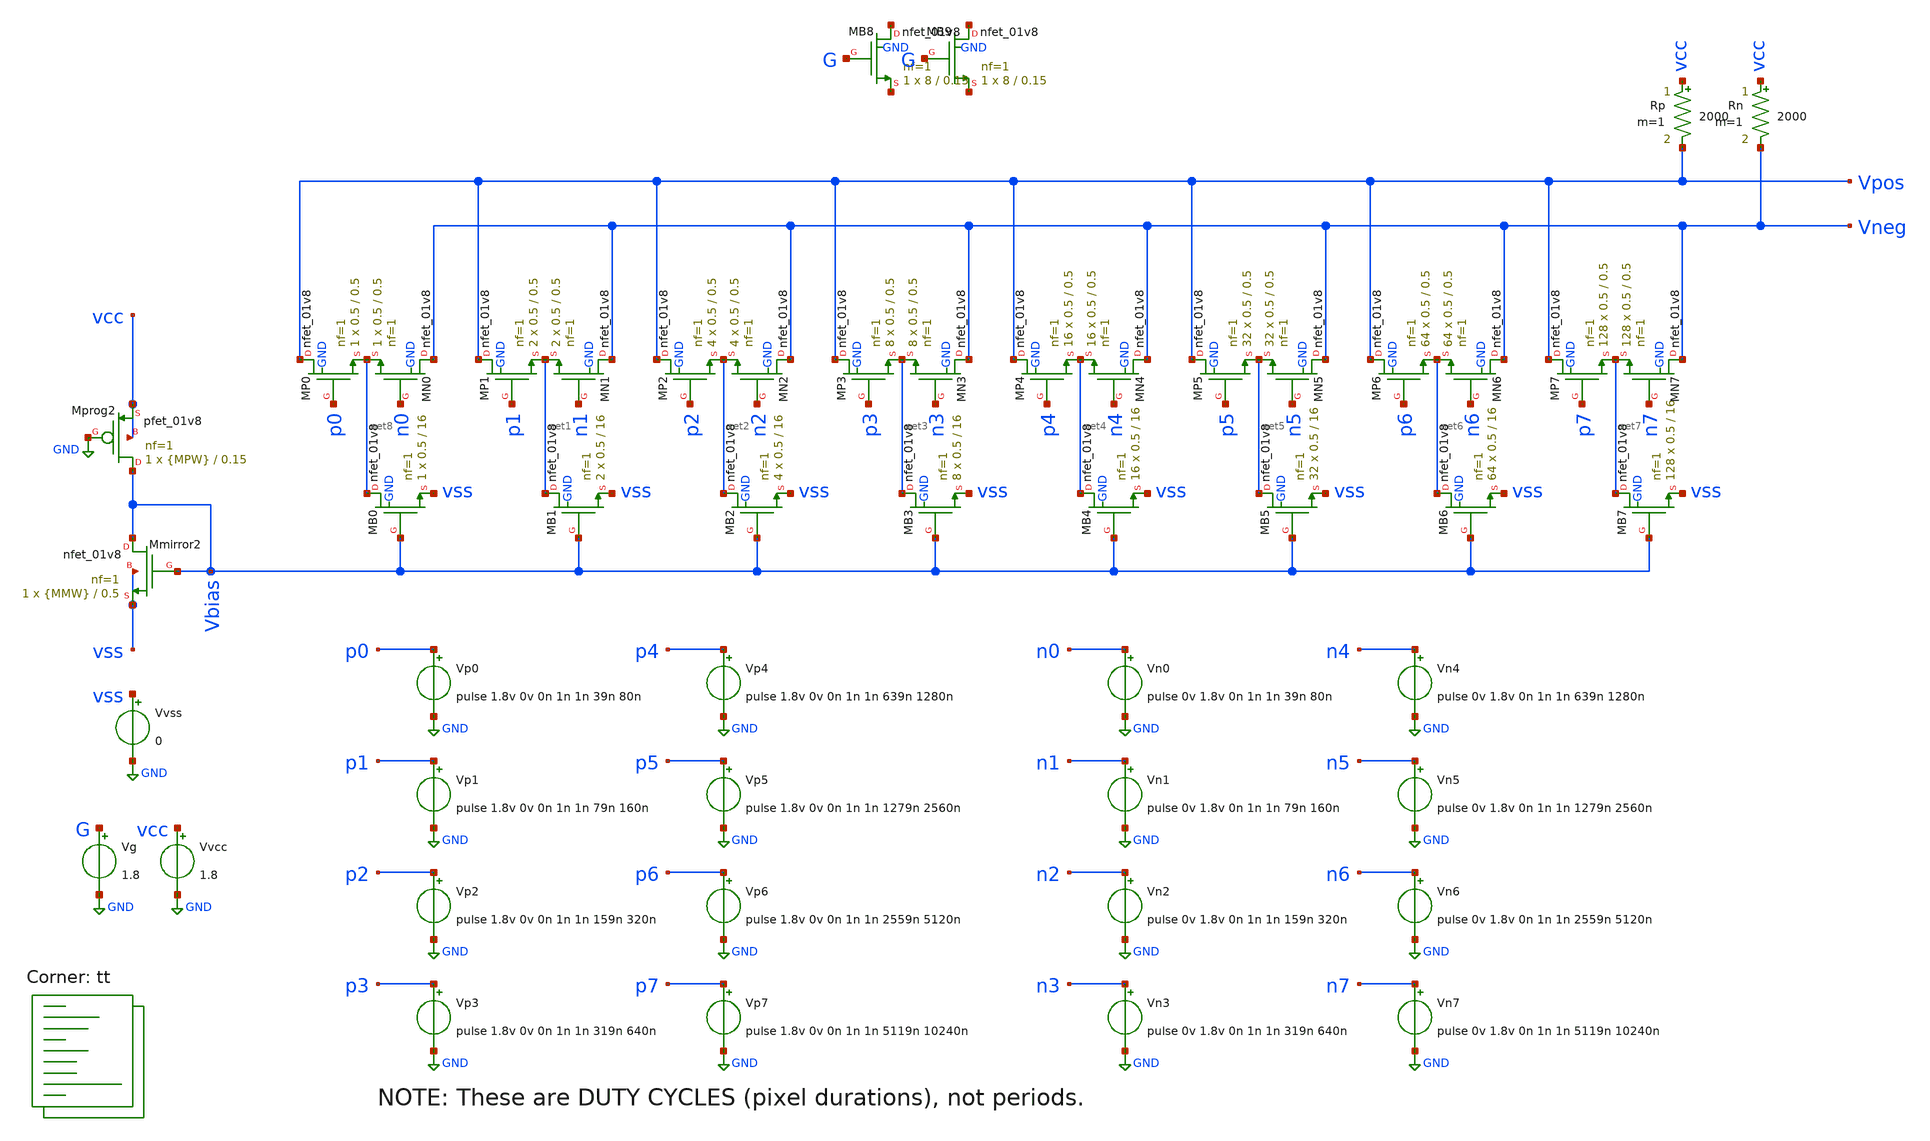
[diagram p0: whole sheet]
** sch_path: xschem/10-steer.sch
**.subckt 10-steer
Vvcc vcc GND 1.8
Vg G GND 1.8
XMprog2 Vbias GND vcc vcc sky130_fd_pr__pfet_01v8 L=0.15 W={MPW} nf=1 ad='int((nf+1)/2) * W/nf * 0.29'
+ as='int((nf+2)/2) * W/nf * 0.29' pd='2*int((nf+1)/2) * (W/nf + 0.29)' ps='2*int((nf+2)/2) * (W/nf + 0.29)'
+ nrd='0.29 / W' nrs='0.29 / W' sa=0 sb=0 sd=0 mult=1 m=1
XMmirror2 Vbias Vbias vss vss sky130_fd_pr__nfet_01v8 L=0.5 W={MMW} nf=1 ad='int((nf+1)/2) * W/nf * 0.29'
+ as='int((nf+2)/2) * W/nf * 0.29' pd='2*int((nf+1)/2) * (W/nf + 0.29)' ps='2*int((nf+2)/2) * (W/nf + 0.29)'
+ nrd='0.29 / W' nrs='0.29 / W' sa=0 sb=0 sd=0 mult=1 m=1
XMB0 net8 Vbias vss GND sky130_fd_pr__nfet_01v8 L=16 W=0.5 nf=1 ad='int((nf+1)/2) * W/nf * 0.29' as='int((nf+2)/2) * W/nf * 0.29'
+ pd='2*int((nf+1)/2) * (W/nf + 0.29)' ps='2*int((nf+2)/2) * (W/nf + 0.29)' nrd='0.29 / W' nrs='0.29 / W'
+ sa=0 sb=0 sd=0 mult=1 m=1
XMP0 Vpos p0 net8 GND sky130_fd_pr__nfet_01v8 L=0.5 W=0.5 nf=1 ad='int((nf+1)/2) * W/nf * 0.29' as='int((nf+2)/2) * W/nf * 0.29'
+ pd='2*int((nf+1)/2) * (W/nf + 0.29)' ps='2*int((nf+2)/2) * (W/nf + 0.29)' nrd='0.29 / W' nrs='0.29 / W'
+ sa=0 sb=0 sd=0 mult=1 m=1
XMN0 Vneg n0 net8 GND sky130_fd_pr__nfet_01v8 L=0.5 W=0.5 nf=1 ad='int((nf+1)/2) * W/nf * 0.29' as='int((nf+2)/2) * W/nf * 0.29'
+ pd='2*int((nf+1)/2) * (W/nf + 0.29)' ps='2*int((nf+2)/2) * (W/nf + 0.29)' nrd='0.29 / W' nrs='0.29 / W'
+ sa=0 sb=0 sd=0 mult=1 m=1
XMB1 net1 Vbias vss GND sky130_fd_pr__nfet_01v8 L=16 W=0.5 nf=1 ad='int((nf+1)/2) * W/nf * 0.29' as='int((nf+2)/2) * W/nf * 0.29'
+ pd='2*int((nf+1)/2) * (W/nf + 0.29)' ps='2*int((nf+2)/2) * (W/nf + 0.29)' nrd='0.29 / W' nrs='0.29 / W'
+ sa=0 sb=0 sd=0 mult=2 m=2
XMP1 Vpos p1 net1 GND sky130_fd_pr__nfet_01v8 L=0.5 W=0.5 nf=1 ad='int((nf+1)/2) * W/nf * 0.29' as='int((nf+2)/2) * W/nf * 0.29'
+ pd='2*int((nf+1)/2) * (W/nf + 0.29)' ps='2*int((nf+2)/2) * (W/nf + 0.29)' nrd='0.29 / W' nrs='0.29 / W'
+ sa=0 sb=0 sd=0 mult=2 m=2
XMN1 Vneg n1 net1 GND sky130_fd_pr__nfet_01v8 L=0.5 W=0.5 nf=1 ad='int((nf+1)/2) * W/nf * 0.29' as='int((nf+2)/2) * W/nf * 0.29'
+ pd='2*int((nf+1)/2) * (W/nf + 0.29)' ps='2*int((nf+2)/2) * (W/nf + 0.29)' nrd='0.29 / W' nrs='0.29 / W'
+ sa=0 sb=0 sd=0 mult=2 m=2
XMB2 net2 Vbias vss GND sky130_fd_pr__nfet_01v8 L=16 W=0.5 nf=1 ad='int((nf+1)/2) * W/nf * 0.29' as='int((nf+2)/2) * W/nf * 0.29'
+ pd='2*int((nf+1)/2) * (W/nf + 0.29)' ps='2*int((nf+2)/2) * (W/nf + 0.29)' nrd='0.29 / W' nrs='0.29 / W'
+ sa=0 sb=0 sd=0 mult=4 m=4
XMP2 Vpos p2 net2 GND sky130_fd_pr__nfet_01v8 L=0.5 W=0.5 nf=1 ad='int((nf+1)/2) * W/nf * 0.29' as='int((nf+2)/2) * W/nf * 0.29'
+ pd='2*int((nf+1)/2) * (W/nf + 0.29)' ps='2*int((nf+2)/2) * (W/nf + 0.29)' nrd='0.29 / W' nrs='0.29 / W'
+ sa=0 sb=0 sd=0 mult=4 m=4
XMN2 Vneg n2 net2 GND sky130_fd_pr__nfet_01v8 L=0.5 W=0.5 nf=1 ad='int((nf+1)/2) * W/nf * 0.29' as='int((nf+2)/2) * W/nf * 0.29'
+ pd='2*int((nf+1)/2) * (W/nf + 0.29)' ps='2*int((nf+2)/2) * (W/nf + 0.29)' nrd='0.29 / W' nrs='0.29 / W'
+ sa=0 sb=0 sd=0 mult=4 m=4
XMB3 net3 Vbias vss GND sky130_fd_pr__nfet_01v8 L=16 W=0.5 nf=1 ad='int((nf+1)/2) * W/nf * 0.29' as='int((nf+2)/2) * W/nf * 0.29'
+ pd='2*int((nf+1)/2) * (W/nf + 0.29)' ps='2*int((nf+2)/2) * (W/nf + 0.29)' nrd='0.29 / W' nrs='0.29 / W'
+ sa=0 sb=0 sd=0 mult=8 m=8
XMP3 Vpos p3 net3 GND sky130_fd_pr__nfet_01v8 L=0.5 W=0.5 nf=1 ad='int((nf+1)/2) * W/nf * 0.29' as='int((nf+2)/2) * W/nf * 0.29'
+ pd='2*int((nf+1)/2) * (W/nf + 0.29)' ps='2*int((nf+2)/2) * (W/nf + 0.29)' nrd='0.29 / W' nrs='0.29 / W'
+ sa=0 sb=0 sd=0 mult=8 m=8
XMN3 Vneg n3 net3 GND sky130_fd_pr__nfet_01v8 L=0.5 W=0.5 nf=1 ad='int((nf+1)/2) * W/nf * 0.29' as='int((nf+2)/2) * W/nf * 0.29'
+ pd='2*int((nf+1)/2) * (W/nf + 0.29)' ps='2*int((nf+2)/2) * (W/nf + 0.29)' nrd='0.29 / W' nrs='0.29 / W'
+ sa=0 sb=0 sd=0 mult=8 m=8
XMB4 net4 Vbias vss GND sky130_fd_pr__nfet_01v8 L=16 W=0.5 nf=1 ad='int((nf+1)/2) * W/nf * 0.29' as='int((nf+2)/2) * W/nf * 0.29'
+ pd='2*int((nf+1)/2) * (W/nf + 0.29)' ps='2*int((nf+2)/2) * (W/nf + 0.29)' nrd='0.29 / W' nrs='0.29 / W'
+ sa=0 sb=0 sd=0 mult=16 m=16
XMP4 Vpos p4 net4 GND sky130_fd_pr__nfet_01v8 L=0.5 W=0.5 nf=1 ad='int((nf+1)/2) * W/nf * 0.29' as='int((nf+2)/2) * W/nf * 0.29'
+ pd='2*int((nf+1)/2) * (W/nf + 0.29)' ps='2*int((nf+2)/2) * (W/nf + 0.29)' nrd='0.29 / W' nrs='0.29 / W'
+ sa=0 sb=0 sd=0 mult=16 m=16
XMN4 Vneg n4 net4 GND sky130_fd_pr__nfet_01v8 L=0.5 W=0.5 nf=1 ad='int((nf+1)/2) * W/nf * 0.29' as='int((nf+2)/2) * W/nf * 0.29'
+ pd='2*int((nf+1)/2) * (W/nf + 0.29)' ps='2*int((nf+2)/2) * (W/nf + 0.29)' nrd='0.29 / W' nrs='0.29 / W'
+ sa=0 sb=0 sd=0 mult=16 m=16
XMB5 net5 Vbias vss GND sky130_fd_pr__nfet_01v8 L=16 W=0.5 nf=1 ad='int((nf+1)/2) * W/nf * 0.29' as='int((nf+2)/2) * W/nf * 0.29'
+ pd='2*int((nf+1)/2) * (W/nf + 0.29)' ps='2*int((nf+2)/2) * (W/nf + 0.29)' nrd='0.29 / W' nrs='0.29 / W'
+ sa=0 sb=0 sd=0 mult=32 m=32
XMP5 Vpos p5 net5 GND sky130_fd_pr__nfet_01v8 L=0.5 W=0.5 nf=1 ad='int((nf+1)/2) * W/nf * 0.29' as='int((nf+2)/2) * W/nf * 0.29'
+ pd='2*int((nf+1)/2) * (W/nf + 0.29)' ps='2*int((nf+2)/2) * (W/nf + 0.29)' nrd='0.29 / W' nrs='0.29 / W'
+ sa=0 sb=0 sd=0 mult=32 m=32
XMN5 Vneg n5 net5 GND sky130_fd_pr__nfet_01v8 L=0.5 W=0.5 nf=1 ad='int((nf+1)/2) * W/nf * 0.29' as='int((nf+2)/2) * W/nf * 0.29'
+ pd='2*int((nf+1)/2) * (W/nf + 0.29)' ps='2*int((nf+2)/2) * (W/nf + 0.29)' nrd='0.29 / W' nrs='0.29 / W'
+ sa=0 sb=0 sd=0 mult=32 m=32
XMB6 net6 Vbias vss GND sky130_fd_pr__nfet_01v8 L=16 W=0.5 nf=1 ad='int((nf+1)/2) * W/nf * 0.29' as='int((nf+2)/2) * W/nf * 0.29'
+ pd='2*int((nf+1)/2) * (W/nf + 0.29)' ps='2*int((nf+2)/2) * (W/nf + 0.29)' nrd='0.29 / W' nrs='0.29 / W'
+ sa=0 sb=0 sd=0 mult=64 m=64
XMP6 Vpos p6 net6 GND sky130_fd_pr__nfet_01v8 L=0.5 W=0.5 nf=1 ad='int((nf+1)/2) * W/nf * 0.29' as='int((nf+2)/2) * W/nf * 0.29'
+ pd='2*int((nf+1)/2) * (W/nf + 0.29)' ps='2*int((nf+2)/2) * (W/nf + 0.29)' nrd='0.29 / W' nrs='0.29 / W'
+ sa=0 sb=0 sd=0 mult=64 m=64
XMN6 Vneg n6 net6 GND sky130_fd_pr__nfet_01v8 L=0.5 W=0.5 nf=1 ad='int((nf+1)/2) * W/nf * 0.29' as='int((nf+2)/2) * W/nf * 0.29'
+ pd='2*int((nf+1)/2) * (W/nf + 0.29)' ps='2*int((nf+2)/2) * (W/nf + 0.29)' nrd='0.29 / W' nrs='0.29 / W'
+ sa=0 sb=0 sd=0 mult=64 m=64
XMB7 net7 Vbias vss GND sky130_fd_pr__nfet_01v8 L=16 W=0.5 nf=1 ad='int((nf+1)/2) * W/nf * 0.29' as='int((nf+2)/2) * W/nf * 0.29'
+ pd='2*int((nf+1)/2) * (W/nf + 0.29)' ps='2*int((nf+2)/2) * (W/nf + 0.29)' nrd='0.29 / W' nrs='0.29 / W'
+ sa=0 sb=0 sd=0 mult=128 m=128
XMP7 Vpos p7 net7 GND sky130_fd_pr__nfet_01v8 L=0.5 W=0.5 nf=1 ad='int((nf+1)/2) * W/nf * 0.29' as='int((nf+2)/2) * W/nf * 0.29'
+ pd='2*int((nf+1)/2) * (W/nf + 0.29)' ps='2*int((nf+2)/2) * (W/nf + 0.29)' nrd='0.29 / W' nrs='0.29 / W'
+ sa=0 sb=0 sd=0 mult=128 m=128
XMN7 Vneg n7 net7 GND sky130_fd_pr__nfet_01v8 L=0.5 W=0.5 nf=1 ad='int((nf+1)/2) * W/nf * 0.29' as='int((nf+2)/2) * W/nf * 0.29'
+ pd='2*int((nf+1)/2) * (W/nf + 0.29)' ps='2*int((nf+2)/2) * (W/nf + 0.29)' nrd='0.29 / W' nrs='0.29 / W'
+ sa=0 sb=0 sd=0 mult=128 m=128
Vp0 p0 GND pulse 1.8v 0v 0n 1n 1n 39n 80n
Vp1 p1 GND pulse 1.8v 0v 0n 1n 1n 79n 160n
Vp2 p2 GND pulse 1.8v 0v 0n 1n 1n 159n 320n
Vp3 p3 GND pulse 1.8v 0v 0n 1n 1n 319n 640n
Vp4 p4 GND pulse 1.8v 0v 0n 1n 1n 639n 1280n
Vp5 p5 GND pulse 1.8v 0v 0n 1n 1n 1279n 2560n
Vp6 p6 GND pulse 1.8v 0v 0n 1n 1n 2559n 5120n
Vp7 p7 GND pulse 1.8v 0v 0n 1n 1n 5119n 10240n
Vn0 n0 GND pulse 0v 1.8v 0n 1n 1n 39n 80n
Vn1 n1 GND pulse 0v 1.8v 0n 1n 1n 79n 160n
Vn2 n2 GND pulse 0v 1.8v 0n 1n 1n 159n 320n
Vn3 n3 GND pulse 0v 1.8v 0n 1n 1n 319n 640n
Vn4 n4 GND pulse 0v 1.8v 0n 1n 1n 639n 1280n
Vn5 n5 GND pulse 0v 1.8v 0n 1n 1n 1279n 2560n
Vn6 n6 GND pulse 0v 1.8v 0n 1n 1n 2559n 5120n
Vn7 n7 GND pulse 0v 1.8v 0n 1n 1n 5119n 10240n
Rp vcc Vpos 2000 m=1
Rn vcc Vneg 2000 m=1
Vvss vss GND 0
XMB8 net9 G net10 GND sky130_fd_pr__nfet_01v8 L=0.15 W=8 nf=1 ad='int((nf+1)/2) * W/nf * 0.29' as='int((nf+2)/2) * W/nf * 0.29'
+ pd='2*int((nf+1)/2) * (W/nf + 0.29)' ps='2*int((nf+2)/2) * (W/nf + 0.29)' nrd='0.29 / W' nrs='0.29 / W'
+ sa=0 sb=0 sd=0 mult=1 m=1
XMB9 net11 G net12 GND sky130_fd_pr__nfet_01v8 L=0.15 W=8 nf=1 ad='int((nf+1)/2) * W/nf * 0.29' as='int((nf+2)/2) * W/nf * 0.29'
+ pd='2*int((nf+1)/2) * (W/nf + 0.29)' ps='2*int((nf+2)/2) * (W/nf + 0.29)' nrd='0.29 / W' nrs='0.29 / W'
+ sa=0 sb=0 sd=0 mult=1 m=1
**** begin user architecture code



.param MPW=6
.param MMW=4
.options savecurrents
.control

  save all
  *reset
  *alterparam MPW=6
  *alterparam MMW=4
  tran 1n 12.8u
  write 10.raw i(vvcc) i(vvss) vpos vneg vbias

  set appendwrite
  alterparam MPW=4
  alterparam MMW=4
  reset
  tran 1n 12.8u
  write 10.raw i(vvcc) i(vvss) vpos vneg vbias

.endc



.lib $::SKYWATER_MODELS/sky130.lib.spice tt
**** end user architecture code
**.ends
.GLOBAL GND
.end
